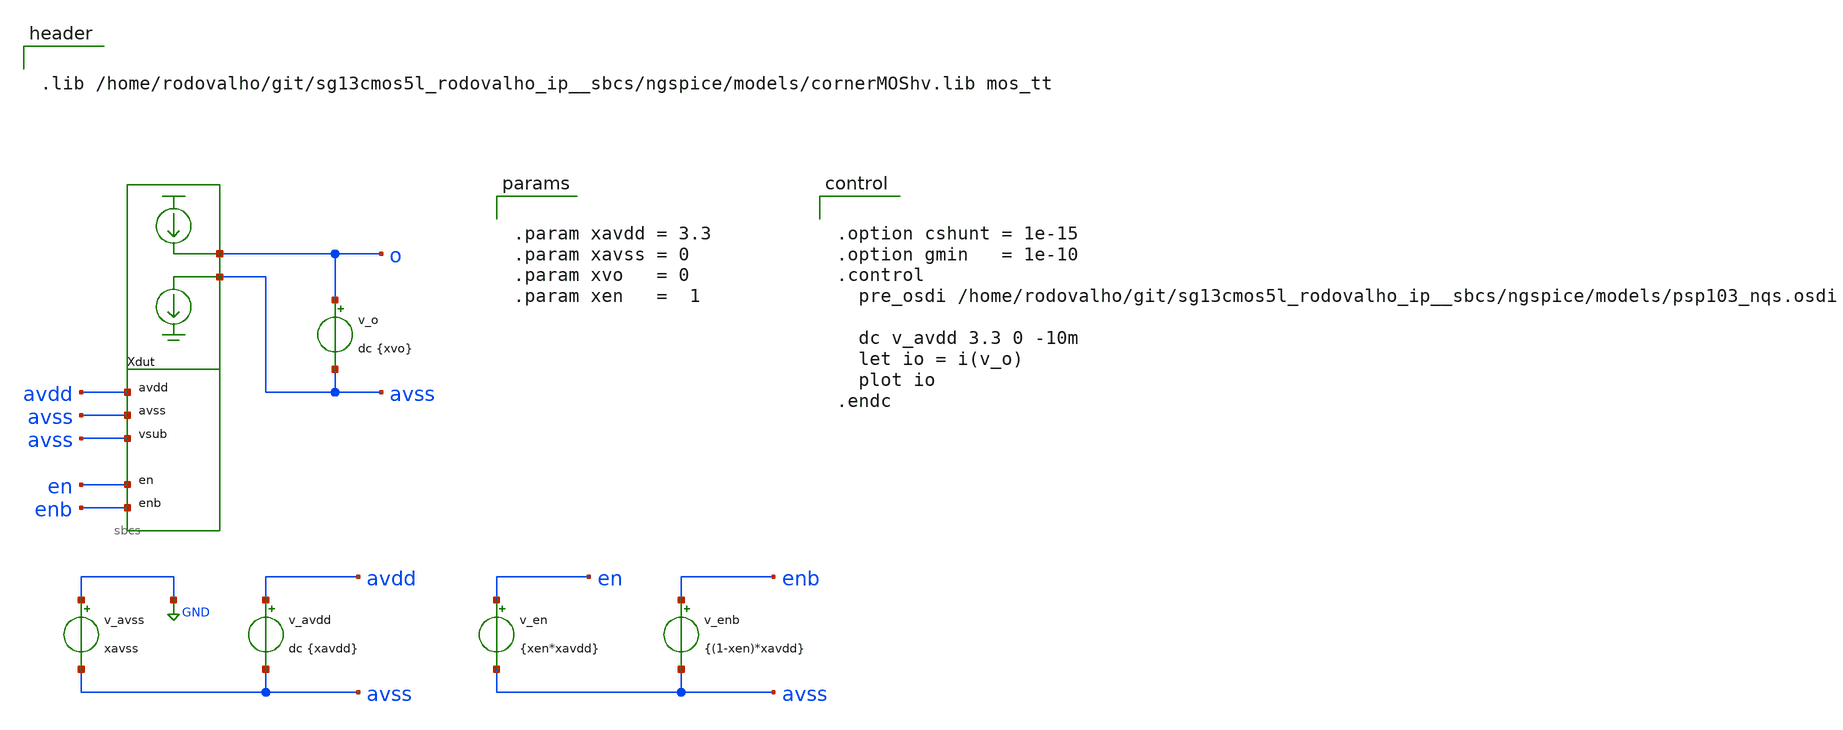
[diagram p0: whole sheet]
** sch_path: xschem/tb_sbcs_vsweep.sch
**.subckt tb_sbcs_vsweep
Xdut o avss avdd avss en enb sbcs
v_avss GND avss xavss
v_avdd avdd avss dc {xavdd}
v_en en avss {xen*xavdd}
v_enb enb avss {(1-xen)*xavdd}
v_o o avss dc {xvo}
**** begin user architecture code


.lib /home/rodovalho/git/sg13cmos5l_rodovalho_ip__sbcs/ngspice/models/cornerMOShv.lib mos_tt




.option cshunt = 1e-15
.option gmin   = 1e-10
.control
  pre_osdi /home/rodovalho/git/sg13cmos5l_rodovalho_ip__sbcs/ngspice/models/psp103_nqs.osdi

  dc v_avdd 3.3 0 -10m
  let io = i(v_o)
  plot io
.endc




.param xavdd = 3.3
.param xavss = 0
.param xvo   = 0
.param xen   =  1


**** end user architecture code
**.ends
.GLOBAL GND
.end
